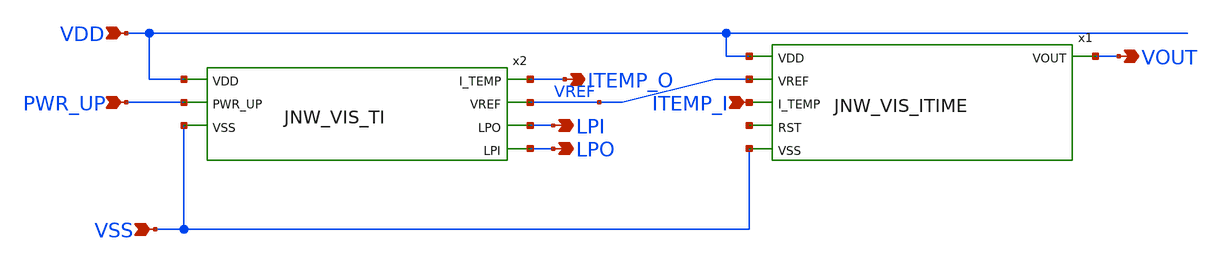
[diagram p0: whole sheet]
** sch_path: design/JNW_GR02_SKY130A/JNW_GR02_VIS.sch
**.subckt JNW_GR02_VIS VDD VSS PWR_UP VOUT LPI LPO ITEMP_O ITEMP_I
*.ipin VDD
*.ipin VSS
*.ipin PWR_UP
*.opin VOUT
*.opin LPI
*.opin LPO
*.opin ITEMP_O
*.ipin ITEMP_I
x1 VDD VREF VOUT ITEMP_I net1 VSS JNW_VIS_ITIME
x2 ITEMP_O VDD VREF LPI LPO PWR_UP VSS JNW_VIS_TI
**.ends
.end
